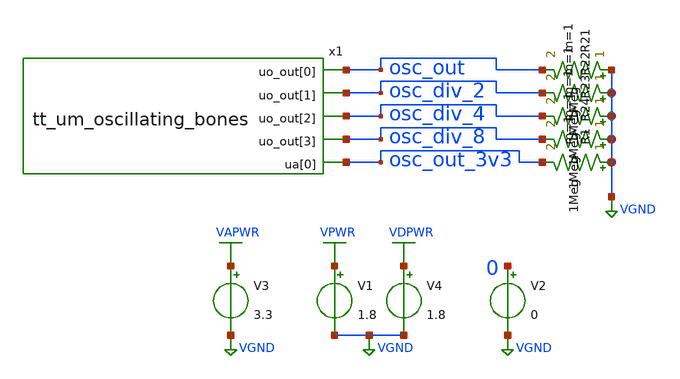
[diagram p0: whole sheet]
** sch_path: xschem/testbench.sch
**.subckt testbench
x1 osc_out osc_div_2 osc_div_4 osc_div_8 osc_out_3v3 tt_um_oscillating_bones
V1 VPWR VGND 1.8
R21 VGND osc_out 1Meg m=1
R22 VGND osc_div_2 1Meg m=1
R23 VGND osc_div_4 1Meg m=1
R24 VGND osc_div_8 1Meg m=1
V2 0 VGND 0
V3 VAPWR VGND 3.3
V4 VDPWR VGND 1.8
R1 VGND osc_out_3v3 1Meg m=1
**** begin user architecture code

** opencircuitdesign pdks install
.lib $::SKYWATER_MODELS/sky130.lib.spice tt
.include $::SKYWATER_STDCELLS/sky130_fd_sc_hd.spice





.tran 50p 200n
.save all

.control
run

meas tran tdiff TRIG osc_out VAL=1.7 RISE=2 TARG osc_out VAL=1.7 RISE=3
let osc_freq_mhz = (1 / (tdiff) / 1e6)
save osc_freq_mhz

meas tran tdiff_div2 TRIG osc_div_2 VAL=1.7 RISE=2 TARG osc_div_2 VAL=1.7 RISE=3
let osc_div_2_freq_mhz = (1 / (tdiff_div2) / 1e6)
save osc_div_2_freq_mhz

meas tran tdiff_div4 TRIG osc_div_4 VAL=1.7 RISE=2 TARG osc_div_4 VAL=1.7 RISE=3
let osc_div_4_freq_mhz = (1 / (tdiff_div4) / 1e6)
save osc_div_4_freq_mhz

meas tran tdiff_div8 TRIG osc_div_8 VAL=1.7 RISE=2 TARG osc_div_8 VAL=1.7 RISE=3
let osc_div_8_freq_mhz = (1 / (tdiff_div8) / 1e6)
save osc_div_8_freq_mhz

write testbench.raw
.endc


**** end user architecture code
**.ends

* expanding   symbol:  tt_um_oscillating_bones.sym # of pins=5
** sym_path: xschem/tt_um_oscillating_bones.sym
** sch_path: xschem/tt_um_oscillating_bones.sch
.subckt tt_um_oscillating_bones uo_out[0] uo_out[1] uo_out[2] uo_out[3] ua[0]
*.opin uo_out[1]
*.opin uo_out[0]
*.opin uo_out[2]
*.opin uo_out[3]
*.opin ua[0]
x22 uo_out[1] uo_out[2] uo_out[3] uo_out[0] freq_divider
x1 net1 ring
x2 net1 uo_out[0] VDPWR skullfet_inverter_5v_pwr
x3 uo_out[0] ua[0] VAPWR skullfet_inverter_5v_pwr
.ends


* expanding   symbol:  freq_divider.sym # of pins=4
** sym_path: xschem/freq_divider.sym
** sch_path: xschem/freq_divider.sch
.subckt freq_divider ODIV2 ODIV4 ODIV8 IN
*.ipin IN
*.opin ODIV2
*.opin ODIV4
*.opin ODIV8
x4 ODIV2 net3 IN net3 VDPWR VDD VSS sg13g2_dfrbp_2
x1 ODIV4 net1 ODIV2 net1 VDPWR VDD VSS sg13g2_dfrbp_2
x2 ODIV8 net2 ODIV4 net2 VDPWR VDD VSS sg13g2_dfrbp_2
.ends


* expanding   symbol:  ring.sym # of pins=1
** sym_path: xschem/ring.sym
** sch_path: xschem/ring.sch
.subckt ring ROSC_OUT
*.opin ROSC_OUT
x1 net20 net1 skullfet_inverter
x2 net1 net3 skullfet_inverter
x3 net3 net2 skullfet_inverter
x4 net2 ROSC_OUT skullfet_inverter
x5 ROSC_OUT net4 skullfet_inverter
x7 net5 net6 skullfet_inverter
x6 net4 net5 skullfet_inverter
x8 net6 net7 skullfet_inverter
x9 net7 net11 skullfet_inverter
x10 net11 net8 skullfet_inverter
x11 net8 net9 skullfet_inverter
x12 net9 net10 skullfet_inverter
x13 net10 net12 skullfet_inverter
x14 net12 net13 skullfet_inverter
x15 net13 net14 skullfet_inverter
x16 net14 net15 skullfet_inverter
x17 net15 net16 skullfet_inverter
x18 net16 net17 skullfet_inverter
x19 net17 net18 skullfet_inverter
x20 net18 net19 skullfet_inverter
x21 net19 net20 skullfet_inverter
.ends


* expanding   symbol:  skullfet_inverter_5v_pwr.sym # of pins=3
** sym_path: xschem/skullfet_inverter_5v_pwr.sym
** sch_path: xschem/skullfet_inverter_5v_pwr.sch
.subckt skullfet_inverter_5v_pwr A Y VDD
*.ipin A
*.opin Y
*.ipin VDD
XM1 Y A VDD VDD sky130_fd_pr__pfet_g5v0d10v5 L=0.5 W=4.5 nf=1 ad=5.3775 as=7.5825 pd=12.07 ps=29.53 nrd='0.29 / 4.5 '
+ nrs='0.29 / 4.5 ' sa=0 sb=0 sd=0 mult=1 m=1
XM2 Y A VGND VGND sky130_fd_pr__nfet_g5v0d10v5 L=0.5 W=4.5 nf=1 ad=7.8525 as=5.1075 pd=29.65 ps=11.95
+ nrd='0.29 / 4.5 ' nrs='0.29 / 4.5 ' sa=0 sb=0 sd=0 mult=1 m=1
.ends


* expanding   symbol:  sg13g2_stdcells/sg13g2_dfrbp_2.sym # of pins=5
** sym_path: sg13g2_stdcells/sg13g2_dfrbp_2.sym
** sch_path: sg13g2_stdcells/sg13g2_dfrbp_2.sch
.subckt sg13g2_dfrbp_2 Q Q_N CLK D RESET_B VDD VSS
*.ipin D
*.ipin RESET_B
*.ipin CLK
*.opin Q
*.opin Q_N
*.iopin VDD
*.iopin VSS
XM1 Db D net12 VSS sg13_lv_nmos w=420.00n l=130.00n ng=1 m=1 mm_ok=1
XM2 net12 RESET_B VSS VSS sg13_lv_nmos w=420.00n l=130.00n ng=1 m=1 mm_ok=1
XM3 net2 clkneg net11 VSS sg13_lv_nmos w=420.00n l=130.00n ng=1 m=1 mm_ok=1
XM4 net11 net3 VSS VSS sg13_lv_nmos w=420.00n l=130.00n ng=1 m=1 mm_ok=1
XM5 net3 net2 net7 VSS sg13_lv_nmos w=420.00n l=130.00n ng=1 m=1 mm_ok=1
XM6 net7 RESET_B VSS VSS sg13_lv_nmos w=420.00n l=130.00n ng=1 m=1 mm_ok=1
XM7 Q_N net2 VSS VSS sg13_lv_nmos w=1.48u l=130.00n ng=2 m=1 mm_ok=1
XM8 net1 net2 VSS VSS sg13_lv_nmos w=640.00n l=130.00n ng=1 m=1 mm_ok=1
XM9 Q net1 VSS VSS sg13_lv_nmos w=1.48u l=130.00n ng=2 m=1 mm_ok=1
XM10 clkneg CLK VSS VSS sg13_lv_nmos w=740.00n l=130.00n ng=1 m=1 mm_ok=1
XM11 clkpos clkneg VSS VSS sg13_lv_nmos w=740.00n l=130.00n ng=1 m=1 mm_ok=1
XM12 Db clkneg net4 VSS sg13_lv_nmos w=420.00n l=130.00n ng=1 m=1 mm_ok=1
XM13 net4 clkpos net10 VSS sg13_lv_nmos w=420.00n l=130.00n ng=1 m=1 mm_ok=1
XM14 net10 net5 net6 VSS sg13_lv_nmos w=420.00n l=130.00n ng=1 m=1 mm_ok=1
XM15 net6 RESET_B VSS VSS sg13_lv_nmos w=420.00n l=130.00n ng=1 m=1 mm_ok=1
XM16 net5 net4 VSS VSS sg13_lv_nmos w=740.00n l=130.00n ng=1 m=1 mm_ok=1
XM17 net5 clkpos net2 VSS sg13_lv_nmos w=740.00n l=130.00n ng=1 m=1 mm_ok=1
XM18 Db RESET_B VDD VDD sg13_lv_pmos w=420.00n l=130.00n ng=1 m=1 mm_ok=1
XM19 Db D VDD VDD sg13_lv_pmos w=420.00n l=130.00n ng=1 m=1 mm_ok=1
XM20 net9 net3 VDD VDD sg13_lv_pmos w=420.00n l=130.00n ng=1 m=1 mm_ok=1
XM21 net2 clkpos net9 VDD sg13_lv_pmos w=420.00n l=130.00n ng=1 m=1 mm_ok=1
XM22 net3 net2 VDD VDD sg13_lv_pmos w=420.00n l=130.00n ng=1 m=1 mm_ok=1
XM23 net3 RESET_B VDD VDD sg13_lv_pmos w=420.00n l=130.00n ng=1 m=1 mm_ok=1
XM24 Q_N net2 VDD VDD sg13_lv_pmos w=2.24u l=130.00n ng=2 m=1 mm_ok=1
XM25 net1 net2 VDD VDD sg13_lv_pmos w=1.000u l=130.00n ng=1 m=1 mm_ok=1
XM26 Q net1 VDD VDD sg13_lv_pmos w=2.24u l=130.00n ng=2 m=1 mm_ok=1
XM27 clkneg CLK VDD VDD sg13_lv_pmos w=1.12u l=130.00n ng=1 m=1 mm_ok=1
XM28 clkpos clkneg VDD VDD sg13_lv_pmos w=1.12u l=130.00n ng=1 m=1 mm_ok=1
XM29 Db clkpos net4 VDD sg13_lv_pmos w=420.00n l=130.00n ng=1 m=1 mm_ok=1
XM30 net8 net5 VDD VDD sg13_lv_pmos w=420.00n l=130.00n ng=1 m=1 mm_ok=1
XM31 net4 clkneg net8 VDD sg13_lv_pmos w=420.00n l=130.00n ng=1 m=1 mm_ok=1
XM32 net4 RESET_B VDD VDD sg13_lv_pmos w=420.00n l=130.00n ng=1 m=1 mm_ok=1
XM33 net5 net4 VDD VDD sg13_lv_pmos w=1.000u l=130.00n ng=1 m=1 mm_ok=1
XM34 net5 clkneg net2 VDD sg13_lv_pmos w=1.000u l=130.00n ng=1 m=1 mm_ok=1
.ends


* expanding   symbol:  skullfet_inverter.sym # of pins=2
** sym_path: xschem/skullfet_inverter.sym
** sch_path: xschem/skullfet_inverter.sch
.subckt skullfet_inverter A Y
*.ipin A
*.opin Y
XM1 Y A VDPWR VDPWR sg13_lv_pmos w=0.15u l=0.13u ng=1 m=1 mm_ok=1
XM2 Y A VGND VGND sg13_lv_nmos w=0.15u l=0.13u ng=1 m=1 mm_ok=1
.ends

.GLOBAL VGND
.GLOBAL VPWR
.GLOBAL VAPWR
.GLOBAL VDPWR
.end
